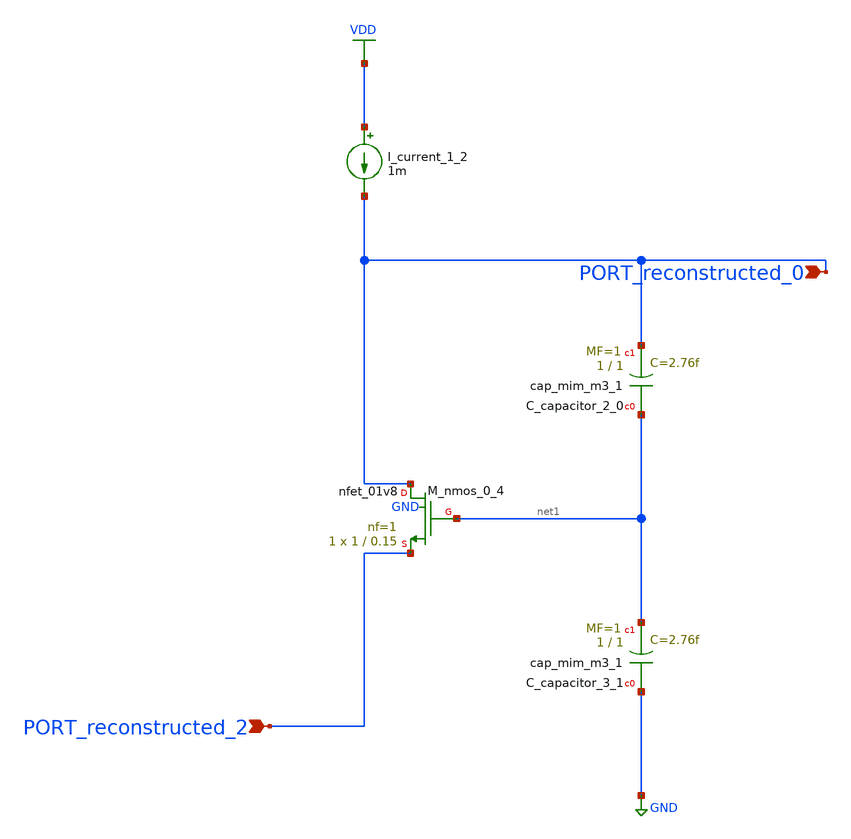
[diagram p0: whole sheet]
** sch_path: schematics/AMSNet/614.sch
**.subckt 614 PORT_reconstructed_2 PORT_reconstructed_0
*.ipin PORT_reconstructed_2
*.ipin PORT_reconstructed_0
XC_capacitor_2_0 net1 PORT_reconstructed_0 sky130_fd_pr__cap_mim_m3_1 W=1 L=1 MF=1 m=1
XC_capacitor_3_1 GND net1 sky130_fd_pr__cap_mim_m3_1 W=1 L=1 MF=1 m=1
I_current_1_2 VDD PORT_reconstructed_0 1m
XM_nmos_0_4 PORT_reconstructed_0 net1 PORT_reconstructed_2 GND sky130_fd_pr__nfet_01v8 L=0.15 W=1 nf=1
+ ad='int((1 + 1)/2) * 1 / 1 * 0.29' as='int((1 + 2)/2) * 1 / 1 * 0.29' pd='2*int((1 + 1)/2) * (1 / 1 + 0.29)'
+ ps='2*int((1 + 2)/2) * (1 / 1 + 0.29)' nrd='0.29 / 1 ' nrs='0.29 / 1 ' sa=0 sb=0 sd=0 mult=1 m=1
**.ends
.GLOBAL GND
.GLOBAL VDD
.end
